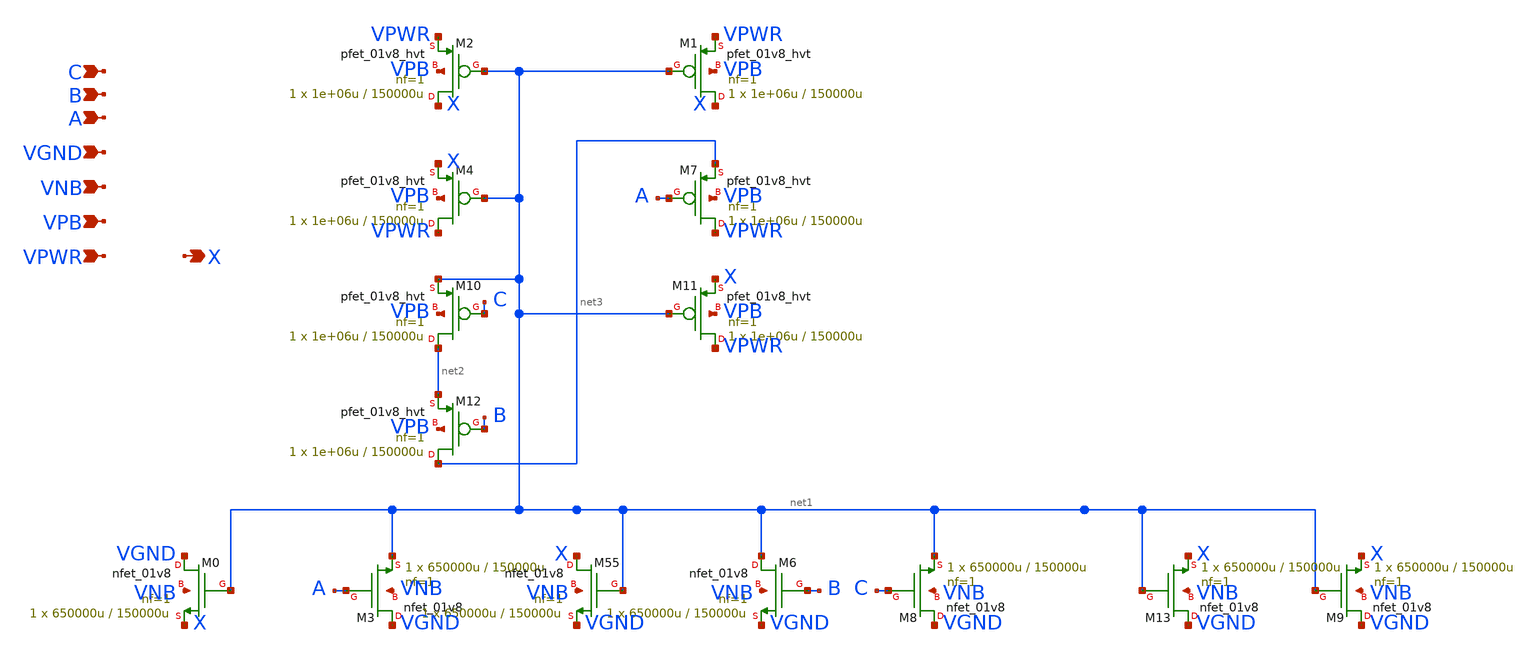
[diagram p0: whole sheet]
** sch_path: schematics/or3/sky130_fd_sc_hd__or3_4.sch
**.subckt sky130_fd_sc_hd__or3_4 A B C VGND VNB VPB VPWR X
*.ipin A
*.ipin B
*.ipin C
*.ipin VGND
*.ipin VNB
*.ipin VPB
*.ipin VPWR
*.opin X
XM6 net1 B VGND VNB sky130_fd_pr__nfet_01v8 L=150000u W=650000u nf=1 ad='int((1 + 1)/2) * 650000u / 1 * 0.29'
+ as='int((1 + 2)/2) * 650000u / 1 * 0.29' pd='2*int((1 + 1)/2) * (650000u / 1 + 0.29)' ps='2*int((1 + 2)/2) * (650000u / 1 + 0.29)'
+ nrd='0.29 / 650000u ' nrs='0.29 / 650000u ' sa=0 sb=0 sd=0 mult=1 m=1
XM1 X net1 VPWR VPB sky130_fd_pr__pfet_01v8_hvt L=150000u W=1e+06u nf=1 ad='int((nf+1)/2) * W/nf * 0.29'
+ as='int((nf+2)/2) * W/nf * 0.29' pd='2*int((nf+1)/2) * (W/nf + 0.29)' ps='2*int((nf+2)/2) * (W/nf + 0.29)'
+ nrd='0.29 / W' nrs='0.29 / W' sa=0 sb=0 sd=0 mult=1 m=1
XM2 X net1 VPWR VPB sky130_fd_pr__pfet_01v8_hvt L=150000u W=1e+06u nf=1 ad='int((nf+1)/2) * W/nf * 0.29'
+ as='int((nf+2)/2) * W/nf * 0.29' pd='2*int((nf+1)/2) * (W/nf + 0.29)' ps='2*int((nf+2)/2) * (W/nf + 0.29)'
+ nrd='0.29 / W' nrs='0.29 / W' sa=0 sb=0 sd=0 mult=1 m=1
XM4 VPWR net1 X VPB sky130_fd_pr__pfet_01v8_hvt L=150000u W=1e+06u nf=1 ad='int((nf+1)/2) * W/nf * 0.29'
+ as='int((nf+2)/2) * W/nf * 0.29' pd='2*int((nf+1)/2) * (W/nf + 0.29)' ps='2*int((nf+2)/2) * (W/nf + 0.29)'
+ nrd='0.29 / W' nrs='0.29 / W' sa=0 sb=0 sd=0 mult=1 m=1
XM7 VPWR A net3 VPB sky130_fd_pr__pfet_01v8_hvt L=150000u W=1e+06u nf=1 ad='int((nf+1)/2) * W/nf * 0.29'
+ as='int((nf+2)/2) * W/nf * 0.29' pd='2*int((nf+1)/2) * (W/nf + 0.29)' ps='2*int((nf+2)/2) * (W/nf + 0.29)'
+ nrd='0.29 / W' nrs='0.29 / W' sa=0 sb=0 sd=0 mult=1 m=1
XM10 net2 C net1 VPB sky130_fd_pr__pfet_01v8_hvt L=150000u W=1e+06u nf=1 ad='int((nf+1)/2) * W/nf * 0.29'
+ as='int((nf+2)/2) * W/nf * 0.29' pd='2*int((nf+1)/2) * (W/nf + 0.29)' ps='2*int((nf+2)/2) * (W/nf + 0.29)'
+ nrd='0.29 / W' nrs='0.29 / W' sa=0 sb=0 sd=0 mult=1 m=1
XM11 VPWR net1 X VPB sky130_fd_pr__pfet_01v8_hvt L=150000u W=1e+06u nf=1 ad='int((nf+1)/2) * W/nf * 0.29'
+ as='int((nf+2)/2) * W/nf * 0.29' pd='2*int((nf+1)/2) * (W/nf + 0.29)' ps='2*int((nf+2)/2) * (W/nf + 0.29)'
+ nrd='0.29 / W' nrs='0.29 / W' sa=0 sb=0 sd=0 mult=1 m=1
XM12 net3 B net2 VPB sky130_fd_pr__pfet_01v8_hvt L=150000u W=1e+06u nf=1 ad='int((nf+1)/2) * W/nf * 0.29'
+ as='int((nf+2)/2) * W/nf * 0.29' pd='2*int((nf+1)/2) * (W/nf + 0.29)' ps='2*int((nf+2)/2) * (W/nf + 0.29)'
+ nrd='0.29 / W' nrs='0.29 / W' sa=0 sb=0 sd=0 mult=1 m=1
XM0 VGND net1 X VNB sky130_fd_pr__nfet_01v8 L=150000u W=650000u nf=1 ad='int((1 + 1)/2) * 650000u / 1 * 0.29'
+ as='int((1 + 2)/2) * 650000u / 1 * 0.29' pd='2*int((1 + 1)/2) * (650000u / 1 + 0.29)' ps='2*int((1 + 2)/2) * (650000u / 1 + 0.29)'
+ nrd='0.29 / 650000u ' nrs='0.29 / 650000u ' sa=0 sb=0 sd=0 mult=1 m=1
XM3 VGND A net1 VNB sky130_fd_pr__nfet_01v8 L=150000u W=650000u nf=1 ad='int((1 + 1)/2) * 650000u / 1 * 0.29'
+ as='int((1 + 2)/2) * 650000u / 1 * 0.29' pd='2*int((1 + 1)/2) * (650000u / 1 + 0.29)' ps='2*int((1 + 2)/2) * (650000u / 1 + 0.29)'
+ nrd='0.29 / 650000u ' nrs='0.29 / 650000u ' sa=0 sb=0 sd=0 mult=1 m=1
XM55 X net1 VGND VNB sky130_fd_pr__nfet_01v8 L=150000u W=650000u nf=1 ad='int((1 + 1)/2) * 650000u / 1 * 0.29'
+ as='int((1 + 2)/2) * 650000u / 1 * 0.29' pd='2*int((1 + 1)/2) * (650000u / 1 + 0.29)' ps='2*int((1 + 2)/2) * (650000u / 1 + 0.29)'
+ nrd='0.29 / 650000u ' nrs='0.29 / 650000u ' sa=0 sb=0 sd=0 mult=1 m=1
XM8 VGND C net1 VNB sky130_fd_pr__nfet_01v8 L=150000u W=650000u nf=1 ad='int((1 + 1)/2) * 650000u / 1 * 0.29'
+ as='int((1 + 2)/2) * 650000u / 1 * 0.29' pd='2*int((1 + 1)/2) * (650000u / 1 + 0.29)' ps='2*int((1 + 2)/2) * (650000u / 1 + 0.29)'
+ nrd='0.29 / 650000u ' nrs='0.29 / 650000u ' sa=0 sb=0 sd=0 mult=1 m=1
XM13 VGND net1 X VNB sky130_fd_pr__nfet_01v8 L=150000u W=650000u nf=1 ad='int((1 + 1)/2) * 650000u / 1 * 0.29'
+ as='int((1 + 2)/2) * 650000u / 1 * 0.29' pd='2*int((1 + 1)/2) * (650000u / 1 + 0.29)' ps='2*int((1 + 2)/2) * (650000u / 1 + 0.29)'
+ nrd='0.29 / 650000u ' nrs='0.29 / 650000u ' sa=0 sb=0 sd=0 mult=1 m=1
XM9 VGND net1 X VNB sky130_fd_pr__nfet_01v8 L=150000u W=650000u nf=1 ad='int((1 + 1)/2) * 650000u / 1 * 0.29'
+ as='int((1 + 2)/2) * 650000u / 1 * 0.29' pd='2*int((1 + 1)/2) * (650000u / 1 + 0.29)' ps='2*int((1 + 2)/2) * (650000u / 1 + 0.29)'
+ nrd='0.29 / 650000u ' nrs='0.29 / 650000u ' sa=0 sb=0 sd=0 mult=1 m=1
**.ends
.end
